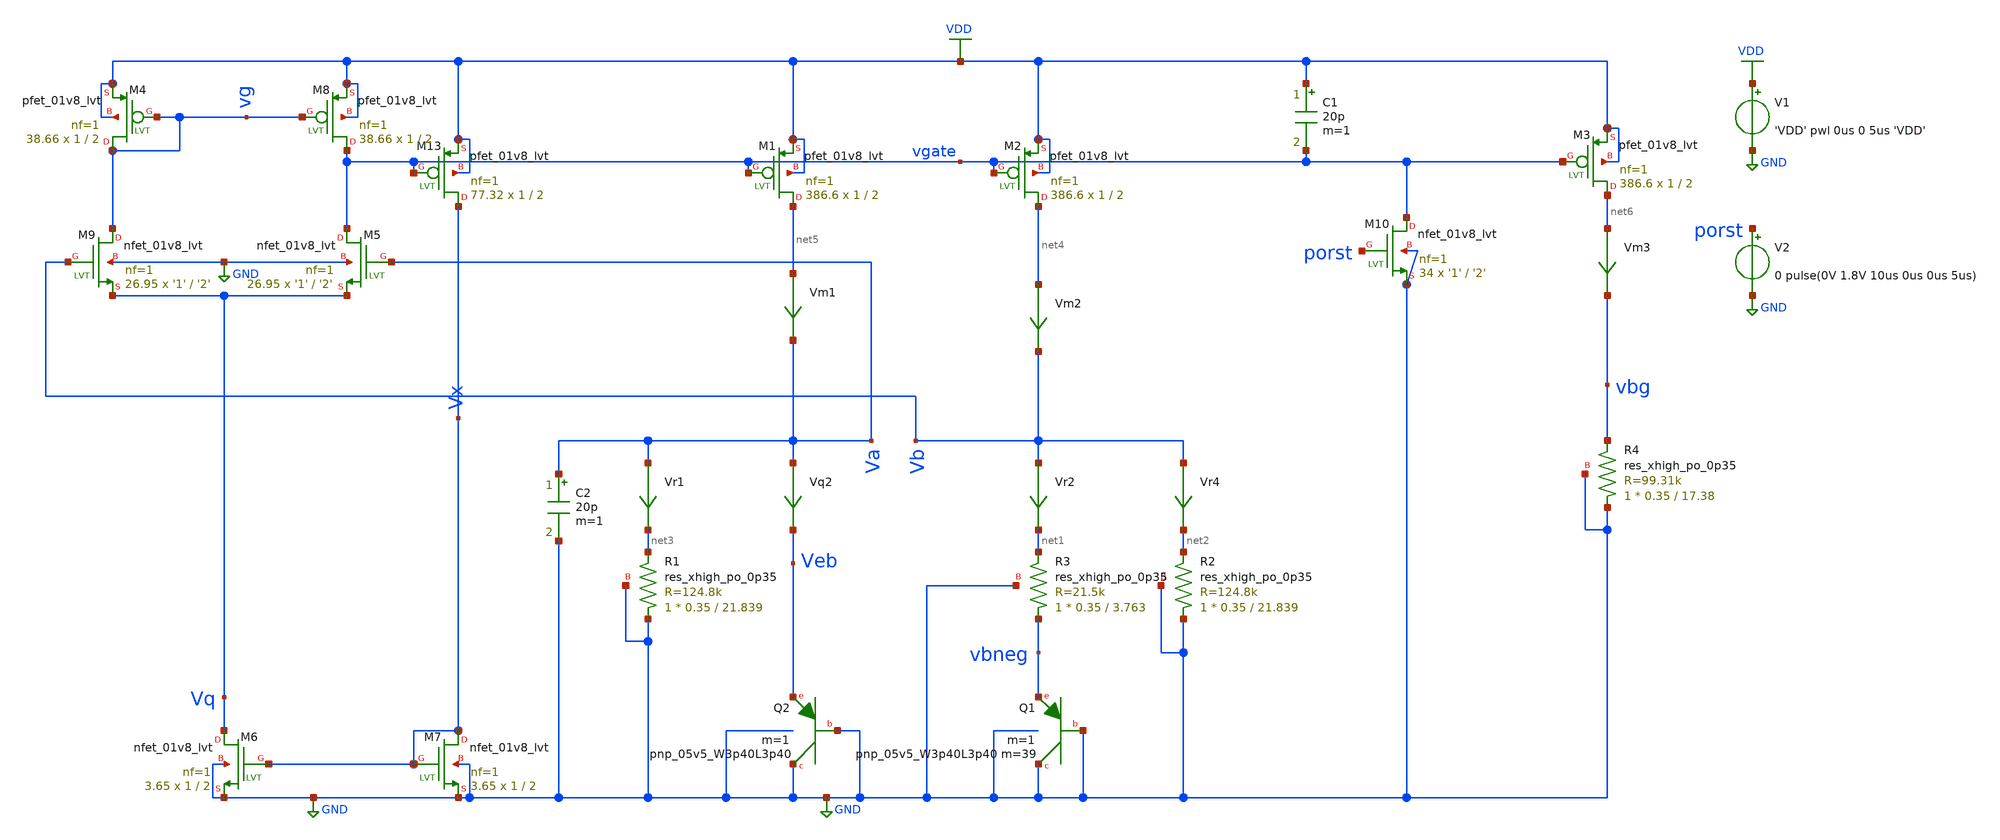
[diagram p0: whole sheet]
** sch_path: schematics/tsmc_bandgap_real_tran_gauss.sch
**.subckt tsmc_bandgap_real_tran_gauss
V1 VDD GND 'VDD' pwl 0us 0 5us 'VDD'
XQ2 GND GND Veb sky130_fd_pr__pnp_05v5_W3p40L3p40 m=1
Vr4 Vb net2 0
.save i(vr4)
Vr2 Vb net1 0
.save i(vr2)
Vm1 net5 Va 0
.save i(vm1)
Vm2 net4 Vb 0
.save i(vm2)
Vm3 net6 vbg 0
.save i(vm3)
Vr1 Va net3 0
.save i(vr1)
Vq2 Va Veb 0
.save i(vq2)
XQ1 GND GND vbneg sky130_fd_pr__pnp_05v5_W3p40L3p40 m=39 m=1
XM5 vgate Va Vq GND sky130_fd_pr__nfet_01v8_lvt L='2' W='1' nf=1 ad='int((nf+1)/2) * W/nf * 0.29' as='int((nf+2)/2) * W/nf * 0.29'
+ pd='2*int((nf+1)/2) * (W/nf + 0.29)' ps='2*int((nf+2)/2) * (W/nf + 0.29)' nrd='0.29 / W' nrs='0.29 / W'
+ sa=0 sb=0 sd=0 mult=26.95 m=26.95
XM6 Vq Vx GND GND sky130_fd_pr__nfet_01v8_lvt L=2 W=1 nf=1 ad='int((nf+1)/2) * W/nf * 0.29' as='int((nf+2)/2) * W/nf * 0.29'
+ pd='2*int((nf+1)/2) * (W/nf + 0.29)' ps='2*int((nf+2)/2) * (W/nf + 0.29)' nrd='0.29 / W' nrs='0.29 / W'
+ sa=0 sb=0 sd=0 mult=3.65 m=3.65
XM9 vg Vb Vq GND sky130_fd_pr__nfet_01v8_lvt L='2' W='1' nf=1 ad='int((nf+1)/2) * W/nf * 0.29' as='int((nf+2)/2) * W/nf * 0.29'
+ pd='2*int((nf+1)/2) * (W/nf + 0.29)' ps='2*int((nf+2)/2) * (W/nf + 0.29)' nrd='0.29 / W' nrs='0.29 / W'
+ sa=0 sb=0 sd=0 mult=26.95 m=26.95
XM7 Vx Vx GND GND sky130_fd_pr__nfet_01v8_lvt L=2 W=1 nf=1 ad='int((nf+1)/2) * W/nf * 0.29' as='int((nf+2)/2) * W/nf * 0.29'
+ pd='2*int((nf+1)/2) * (W/nf + 0.29)' ps='2*int((nf+2)/2) * (W/nf + 0.29)' nrd='0.29 / W' nrs='0.29 / W'
+ sa=0 sb=0 sd=0 mult=3.65 m=3.65
XM13 Vx vgate VDD VDD sky130_fd_pr__pfet_01v8_lvt L=2 W=1 nf=1 ad='int((nf+1)/2) * W/nf * 0.29' as='int((nf+2)/2) * W/nf * 0.29'
+ pd='2*int((nf+1)/2) * (W/nf + 0.29)' ps='2*int((nf+2)/2) * (W/nf + 0.29)' nrd='0.29 / W' nrs='0.29 / W'
+ sa=0 sb=0 sd=0 mult=77.32 m=77.32
XM1 net5 vgate VDD VDD sky130_fd_pr__pfet_01v8_lvt L=2 W=1 nf=1 ad='int((nf+1)/2) * W/nf * 0.29' as='int((nf+2)/2) * W/nf * 0.29'
+ pd='2*int((nf+1)/2) * (W/nf + 0.29)' ps='2*int((nf+2)/2) * (W/nf + 0.29)' nrd='0.29 / W' nrs='0.29 / W'
+ sa=0 sb=0 sd=0 mult=386.6 m=386.6
XM2 net4 vgate VDD VDD sky130_fd_pr__pfet_01v8_lvt L=2 W=1 nf=1 ad='int((nf+1)/2) * W/nf * 0.29' as='int((nf+2)/2) * W/nf * 0.29'
+ pd='2*int((nf+1)/2) * (W/nf + 0.29)' ps='2*int((nf+2)/2) * (W/nf + 0.29)' nrd='0.29 / W' nrs='0.29 / W'
+ sa=0 sb=0 sd=0 mult=386.6 m=386.6
XM3 net6 vgate VDD VDD sky130_fd_pr__pfet_01v8_lvt L=2 W=1 nf=1 ad='int((nf+1)/2) * W/nf * 0.29' as='int((nf+2)/2) * W/nf * 0.29'
+ pd='2*int((nf+1)/2) * (W/nf + 0.29)' ps='2*int((nf+2)/2) * (W/nf + 0.29)' nrd='0.29 / W' nrs='0.29 / W'
+ sa=0 sb=0 sd=0 mult=386.6 m=386.6
XR1 GND net3 GND sky130_fd_pr__res_xhigh_po_0p35 L=21.839 mult=1 m=1
XR2 GND net2 GND sky130_fd_pr__res_xhigh_po_0p35 L=21.839 mult=1 m=1
XR3 vbneg net1 GND sky130_fd_pr__res_xhigh_po_0p35 L=3.763 mult=1 m=1
XR4 GND vbg GND sky130_fd_pr__res_xhigh_po_0p35 L=17.38 mult=1 m=1
XM4 vg vg VDD VDD sky130_fd_pr__pfet_01v8_lvt L=2 W=1 nf=1 ad='int((nf+1)/2) * W/nf * 0.29' as='int((nf+2)/2) * W/nf * 0.29'
+ pd='2*int((nf+1)/2) * (W/nf + 0.29)' ps='2*int((nf+2)/2) * (W/nf + 0.29)' nrd='0.29 / W' nrs='0.29 / W'
+ sa=0 sb=0 sd=0 mult=38.66 m=38.66
XM8 vgate vg VDD VDD sky130_fd_pr__pfet_01v8_lvt L=2 W=1 nf=1 ad='int((nf+1)/2) * W/nf * 0.29' as='int((nf+2)/2) * W/nf * 0.29'
+ pd='2*int((nf+1)/2) * (W/nf + 0.29)' ps='2*int((nf+2)/2) * (W/nf + 0.29)' nrd='0.29 / W' nrs='0.29 / W'
+ sa=0 sb=0 sd=0 mult=38.66 m=38.66
XM10 vgate porst GND GND sky130_fd_pr__nfet_01v8_lvt L='2' W='1' nf=1 ad='int((nf+1)/2) * W/nf * 0.29'
+ as='int((nf+2)/2) * W/nf * 0.29' pd='2*int((nf+1)/2) * (W/nf + 0.29)' ps='2*int((nf+2)/2) * (W/nf + 0.29)'
+ nrd='0.29 / W' nrs='0.29 / W' sa=0 sb=0 sd=0 mult=34 m=34
V2 porst GND 0 pulse(0V 1.8V 10us 0us 0us 5us)
C1 VDD vgate 20p m=1
C2 Va GND 20p m=1
**** begin user architecture code
 .option wnflag=1
.param mc_pr_switch=1.0
.lib /farmshare/home/classes/ee/372/PDKs/share/pdk/sky130A/libs.tech/ngspice/sky130.lib.spice tt


.option seed=13

.param ABSVAR=0.03
.param VDDGAUSS=agauss(1.8, 'ABSVAR', 1)
.param VDD=VDDGAUSS
*.param VDD=1.8
** variation parameters:
.param sky130_fd_pr__nfet_01v8_lvt__vth0_slope_spectre='agauss(0, ABSVAR, 3)/sky130_fd_pr__nfet_01v8_lvt__vth0_slope'
.param sky130_fd_pr__pfet_01v8_lvt__vth0_slope_spectre='agauss(0, ABSVAR, 3)/sky130_fd_pr__pfet_01v8_lvt__vth0_slope'
.param sky130_fd_pr__pfet_01v8_lvt__toxe_slope_spectre='agauss(0, ABSVAR*2, 3)/sky130_fd_pr__pfet_01v8_lvt__toxe_slope'
.param sky130_fd_pr__nfet_01v8_lvt__toxe_slope_spectre='agauss(0, ABSVAR*2, 3)/sky130_fd_pr__nfet_01v8_lvt__toxe_slope'
.param sky130_fd_pr__pfet_01v8_lvt__voff_slope_spectre='agauss(0, ABSVAR, 3)/sky130_fd_pr__pfet_01v8_lvt__voff_slope'
.param sky130_fd_pr__nfet_01v8_lvt__voff_slope_spectre='agauss(0, ABSVAR, 3)/sky130_fd_pr__nfet_01v8_lvt__voff_slope'
.param sky130_fd_pr__pfet_01v8_lvt__nfactor_slope_spectre='agauss(0, ABSVAR, 3)/sky130_fd_pr__pfet_01v8_lvt__nfactor_slope'
.param sky130_fd_pr__nfet_01v8_lvt__nfactor_slope_spectre='agauss(0, ABSVAR, 3)/sky130_fd_pr__nfet_01v8_lvt__nfactor_slope'

.param sky130_fd_pr__res_xhigh_po__var_mult=agauss(0, 'ABSVAR*8', 1)
.param sky130_fd_pr__res_high_po_var=agauss(0, 'ABSVAR*8', 1)

.param sky130_fd_pr__pnp_05v5_W3p40L3p40__bf_slope=agauss(0, 0.05537, 1)
.param sky130_fd_pr__pnp_05v5_W3p40L3p40__is_slope=agauss(0, 0.01662, 1)
.param sky130_fd_pr__pnp_05v5_W3p40L3p40__xti_slope=agauss(0, 0.06, 1)
* .options savecurrents
.control
  let run=1
  dowhile run <= 40
    *print $sky130_fd_pr__nfet_01v8_lvt__vth0_slope_spectre
    if run > 1
      reset
      set appendwrite
    end
    save all
    if run % 3 = 0
      set temp=0
    end
    if run % 3 = 1
      set temp=27
    end
    if run % 3 = 2
      set temp=70
    end
    tran 0.05u 150u
    write ./simulations/tsmc_bandgap_real_tran_gauss{$&run}.raw vbg vdd
    let run = run + 1
    reset
  end
  set nolegend
  *plot all.vbg
  unset askquit
  quit
.endc


**** end user architecture code
**.ends
.GLOBAL VDD
.GLOBAL GND
.end
